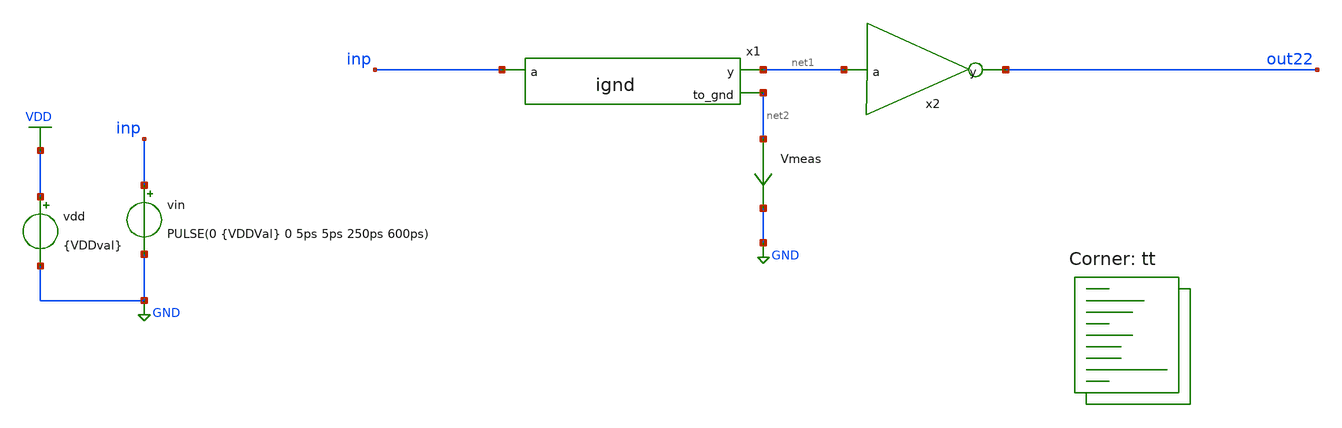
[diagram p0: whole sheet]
** sch_path: assignments/assignment3/assign1c.sch
**.subckt assign1c
vin inp GND PULSE(0 {VDDVal} 0 5ps 5ps 250ps 600ps)
x1 net1 inp net2 ignd
x2 out22 net1 inverter
Vmeas net2 GND 0
.save i(vmeas)
vdd VDD GND {VDDval}
**** begin user architecture code


.param VDDVal = 1.8
.param width_p = 0.84

.save all

.control
let Nsim = 9
let edpvec = vector(Nsim)
let edpvec_ana = vector(Nsim)
let vddvec = vector(Nsim)
let index = 0

* Analytical Constants from your notes
let Ctot = 3.8e-15
let Vtn = 0.7
let Vtp = 0.7
let EcnLn = 0.96
let EcpLp = 1.0
let Kn_WL = 5.838e-4
let Kp_WL = 4.112e-4

while index < Nsim
  let vddv = 1.0 + (index * 0.1)
  let vby2 = vddv / 2

  alterparam VDDVal = $&vddv
  reset
  tran 1p 600p

  * 1. Simulated Delay & Energy
  meas tran thl trig v(inp) val=$&vby2 rise=1 targ v(net1) val=$&vby2 fall=1
  meas tran tlh trig v(inp) val=$&vby2 fall=1 targ v(net1) val=$&vby2 rise=1
  let tp_sim = (thl + tlh) / 2

  * Integrate current to get Charge (Q), then Energy = Q * VDD
  meas tran iinteg integ i(vmeas)
  let edpvec[index] = abs(iinteg) * vddv * tp_sim

  * 2. Analytical Delay & Energy
  let num_hl = Ctot * vby2 * (EcnLn + vddv - Vtn)
  let den_hl = Kn_WL * EcnLn * (vddv - Vtn) * (vddv - Vtn)
  let tphl_ana = num_hl / den_hl

  let num_lh = Ctot * vby2 * (EcpLp + vddv - Vtp)
  let den_lh = Kp_WL * EcpLp * (vddv - Vtp) * (vddv - Vtp)
  let tplh_ana = num_lh / den_lh

  let tp_ana = (tphl_ana + tplh_ana) / 2

  * Analytical EDP = (C * VDD^2) * tp
  let edpvec_ana[index] = (Ctot * vddv * vddv) * tp_ana

  let vddvec[index] = vddv
  let index = index + 1
end

* Plot Simulated vs Analytical EDP
plot edpvec edpvec_ana vs vddvec
.endc


.lib $::SKYWATER_MODELS/sky130.lib.spice tt
**** end user architecture code
**.ends
.GLOBAL GND
.GLOBAL VDD
.end
